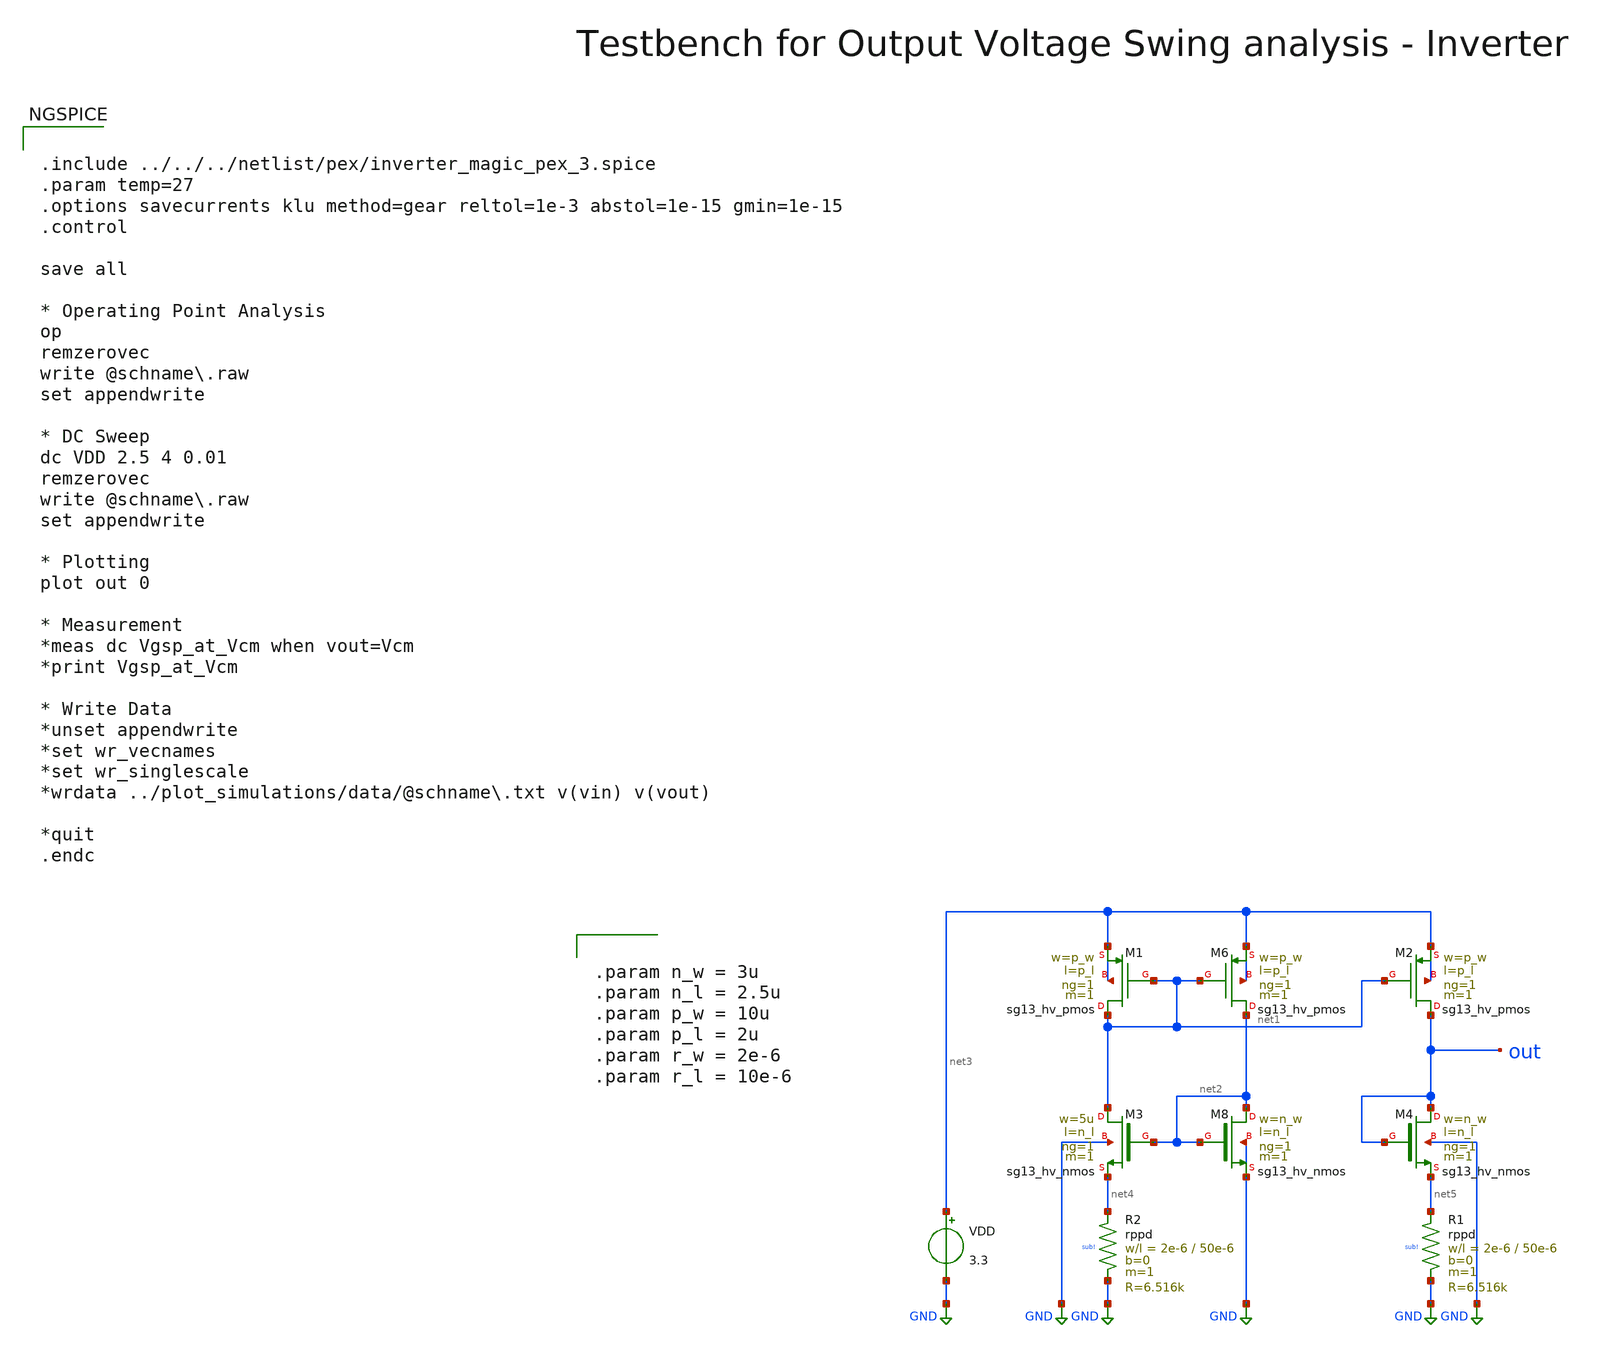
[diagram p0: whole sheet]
** sch_path: macros/heichips26_vcr/macros/switched_capacitor/testbenches/xschem/tb_bandgap_reference_dc.sch
**.subckt tb_bandgap_reference_dc
VDD net3 GND 3.3
XM8 net2 net2 GND GND sg13_hv_nmos w=n_w l=n_l ng=1 m=1 mm_ok=1
XM6 net2 net1 net3 net3 sg13_hv_pmos w=p_w l=p_l ng=1 m=1 mm_ok=1
XM1 net1 net1 net3 net3 sg13_hv_pmos w=p_w l=p_l ng=1 m=1 mm_ok=1
XM2 out net1 net3 net3 sg13_hv_pmos w=p_w l=p_l ng=1 m=1 mm_ok=1
XM3 net1 net2 net4 GND sg13_hv_nmos w=5u l=n_l ng=1 m=1 mm_ok=1
XM4 out out net5 GND sg13_hv_nmos w=n_w l=n_l ng=1 m=1 mm_ok=1
XR1 net5 GND sub! rppd w=2e-6 l=50e-6 m=1 b=0 mm_ok=1
XR2 net4 GND sub! rppd w=2e-6 l=50e-6 m=1 b=0 mm_ok=1
**** begin user architecture code


.include ../../../netlist/pex/inverter_magic_pex_3.spice
.param temp=27
.options savecurrents klu method=gear reltol=1e-3 abstol=1e-15 gmin=1e-15
.control

save all

* Operating Point Analysis
op
remzerovec
write @schname\.raw
set appendwrite

* DC Sweep
dc VDD 2.5 4 0.01
remzerovec
write @schname\.raw
set appendwrite

* Plotting
plot out 0

* Measurement
*meas dc Vgsp_at_Vcm when vout=Vcm
*print Vgsp_at_Vcm

* Write Data
*unset appendwrite
*set wr_vecnames
*set wr_singlescale
*wrdata ../plot_simulations/data/@schname\.txt v(vin) v(vout)

*quit
.endc



.lib cornerMOSlv.lib mos_tt
.lib cornerMOShv.lib mos_tt
.lib cornerRES.lib res_typ
.lib cornerDIO.lib dio_tt



.param n_w = 3u
.param n_l = 2.5u
.param p_w = 10u
.param p_l = 2u
.param r_w = 2e-6
.param r_l = 10e-6


**** end user architecture code
**.ends
.GLOBAL GND
.end
